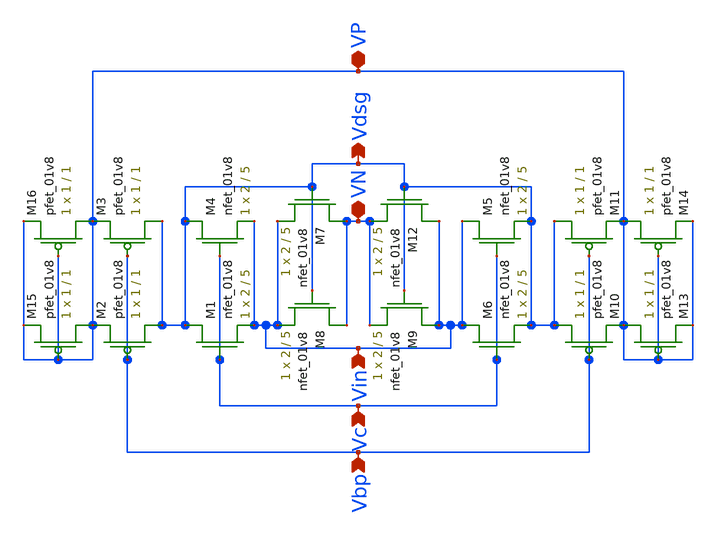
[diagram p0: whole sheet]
** sch_path: LDS/LDS_fvf.sch
**.subckt LDS_fvf VN Vin Vc Vdsg Vbp VP
*.iopin VN
*.ipin Vin
*.ipin Vc
*.opin Vdsg
*.ipin Vbp
*.iopin VP
XM1 Vdsg Vc Vin VN sky130_fd_pr__nfet_01v8 L=5 W=2 nf=1 ad='int((nf+1)/2) * W/nf * 0.29' as='int((nf+2)/2) * W/nf * 0.29'
+ pd='2*int((nf+1)/2) * (W/nf + 0.29)' ps='2*int((nf+2)/2) * (W/nf + 0.29)' nrd='0.29 / W' nrs='0.29 / W'
+ sa=0 sb=0 sd=0 mult=1 m=1
XM2 Vdsg Vbp VP VP sky130_fd_pr__pfet_01v8 L=1 W=1 nf=1 ad='int((nf+1)/2) * W/nf * 0.29' as='int((nf+2)/2) * W/nf * 0.29'
+ pd='2*int((nf+1)/2) * (W/nf + 0.29)' ps='2*int((nf+2)/2) * (W/nf + 0.29)' nrd='0.29 / W' nrs='0.29 / W'
+ sa=0 sb=0 sd=0 mult=1 m=1
XM3 Vdsg Vbp VP VP sky130_fd_pr__pfet_01v8 L=1 W=1 nf=1 ad='int((nf+1)/2) * W/nf * 0.29' as='int((nf+2)/2) * W/nf * 0.29'
+ pd='2*int((nf+1)/2) * (W/nf + 0.29)' ps='2*int((nf+2)/2) * (W/nf + 0.29)' nrd='0.29 / W' nrs='0.29 / W'
+ sa=0 sb=0 sd=0 mult=1 m=1
XM10 Vdsg Vbp VP VP sky130_fd_pr__pfet_01v8 L=1 W=1 nf=1 ad='int((nf+1)/2) * W/nf * 0.29' as='int((nf+2)/2) * W/nf * 0.29'
+ pd='2*int((nf+1)/2) * (W/nf + 0.29)' ps='2*int((nf+2)/2) * (W/nf + 0.29)' nrd='0.29 / W' nrs='0.29 / W'
+ sa=0 sb=0 sd=0 mult=1 m=1
XM11 Vdsg Vbp VP VP sky130_fd_pr__pfet_01v8 L=1 W=1 nf=1 ad='int((nf+1)/2) * W/nf * 0.29' as='int((nf+2)/2) * W/nf * 0.29'
+ pd='2*int((nf+1)/2) * (W/nf + 0.29)' ps='2*int((nf+2)/2) * (W/nf + 0.29)' nrd='0.29 / W' nrs='0.29 / W'
+ sa=0 sb=0 sd=0 mult=1 m=1
XM4 Vdsg Vc Vin VN sky130_fd_pr__nfet_01v8 L=5 W=2 nf=1 ad='int((nf+1)/2) * W/nf * 0.29' as='int((nf+2)/2) * W/nf * 0.29'
+ pd='2*int((nf+1)/2) * (W/nf + 0.29)' ps='2*int((nf+2)/2) * (W/nf + 0.29)' nrd='0.29 / W' nrs='0.29 / W'
+ sa=0 sb=0 sd=0 mult=1 m=1
XM5 Vin Vc Vdsg VN sky130_fd_pr__nfet_01v8 L=5 W=2 nf=1 ad='int((nf+1)/2) * W/nf * 0.29' as='int((nf+2)/2) * W/nf * 0.29'
+ pd='2*int((nf+1)/2) * (W/nf + 0.29)' ps='2*int((nf+2)/2) * (W/nf + 0.29)' nrd='0.29 / W' nrs='0.29 / W'
+ sa=0 sb=0 sd=0 mult=1 m=1
XM6 Vin Vc Vdsg VN sky130_fd_pr__nfet_01v8 L=5 W=2 nf=1 ad='int((nf+1)/2) * W/nf * 0.29' as='int((nf+2)/2) * W/nf * 0.29'
+ pd='2*int((nf+1)/2) * (W/nf + 0.29)' ps='2*int((nf+2)/2) * (W/nf + 0.29)' nrd='0.29 / W' nrs='0.29 / W'
+ sa=0 sb=0 sd=0 mult=1 m=1
XM7 VN Vdsg Vin VN sky130_fd_pr__nfet_01v8 L=5 W=2 nf=1 ad='int((nf+1)/2) * W/nf * 0.29' as='int((nf+2)/2) * W/nf * 0.29'
+ pd='2*int((nf+1)/2) * (W/nf + 0.29)' ps='2*int((nf+2)/2) * (W/nf + 0.29)' nrd='0.29 / W' nrs='0.29 / W'
+ sa=0 sb=0 sd=0 mult=1 m=1
XM8 VN Vdsg Vin VN sky130_fd_pr__nfet_01v8 L=5 W=2 nf=1 ad='int((nf+1)/2) * W/nf * 0.29' as='int((nf+2)/2) * W/nf * 0.29'
+ pd='2*int((nf+1)/2) * (W/nf + 0.29)' ps='2*int((nf+2)/2) * (W/nf + 0.29)' nrd='0.29 / W' nrs='0.29 / W'
+ sa=0 sb=0 sd=0 mult=1 m=1
XM9 Vin Vdsg VN VN sky130_fd_pr__nfet_01v8 L=5 W=2 nf=1 ad='int((nf+1)/2) * W/nf * 0.29' as='int((nf+2)/2) * W/nf * 0.29'
+ pd='2*int((nf+1)/2) * (W/nf + 0.29)' ps='2*int((nf+2)/2) * (W/nf + 0.29)' nrd='0.29 / W' nrs='0.29 / W'
+ sa=0 sb=0 sd=0 mult=1 m=1
XM12 Vin Vdsg VN VN sky130_fd_pr__nfet_01v8 L=5 W=2 nf=1 ad='int((nf+1)/2) * W/nf * 0.29' as='int((nf+2)/2) * W/nf * 0.29'
+ pd='2*int((nf+1)/2) * (W/nf + 0.29)' ps='2*int((nf+2)/2) * (W/nf + 0.29)' nrd='0.29 / W' nrs='0.29 / W'
+ sa=0 sb=0 sd=0 mult=1 m=1
XM13 VP VP VP VP sky130_fd_pr__pfet_01v8 L=1 W=1 nf=1 ad='int((nf+1)/2) * W/nf * 0.29' as='int((nf+2)/2) * W/nf * 0.29'
+ pd='2*int((nf+1)/2) * (W/nf + 0.29)' ps='2*int((nf+2)/2) * (W/nf + 0.29)' nrd='0.29 / W' nrs='0.29 / W'
+ sa=0 sb=0 sd=0 mult=1 m=1
XM14 VP VP VP VP sky130_fd_pr__pfet_01v8 L=1 W=1 nf=1 ad='int((nf+1)/2) * W/nf * 0.29' as='int((nf+2)/2) * W/nf * 0.29'
+ pd='2*int((nf+1)/2) * (W/nf + 0.29)' ps='2*int((nf+2)/2) * (W/nf + 0.29)' nrd='0.29 / W' nrs='0.29 / W'
+ sa=0 sb=0 sd=0 mult=1 m=1
XM15 VP VP VP VP sky130_fd_pr__pfet_01v8 L=1 W=1 nf=1 ad='int((nf+1)/2) * W/nf * 0.29' as='int((nf+2)/2) * W/nf * 0.29'
+ pd='2*int((nf+1)/2) * (W/nf + 0.29)' ps='2*int((nf+2)/2) * (W/nf + 0.29)' nrd='0.29 / W' nrs='0.29 / W'
+ sa=0 sb=0 sd=0 mult=1 m=1
XM16 VP VP VP VP sky130_fd_pr__pfet_01v8 L=1 W=1 nf=1 ad='int((nf+1)/2) * W/nf * 0.29' as='int((nf+2)/2) * W/nf * 0.29'
+ pd='2*int((nf+1)/2) * (W/nf + 0.29)' ps='2*int((nf+2)/2) * (W/nf + 0.29)' nrd='0.29 / W' nrs='0.29 / W'
+ sa=0 sb=0 sd=0 mult=1 m=1
**.ends
.end
